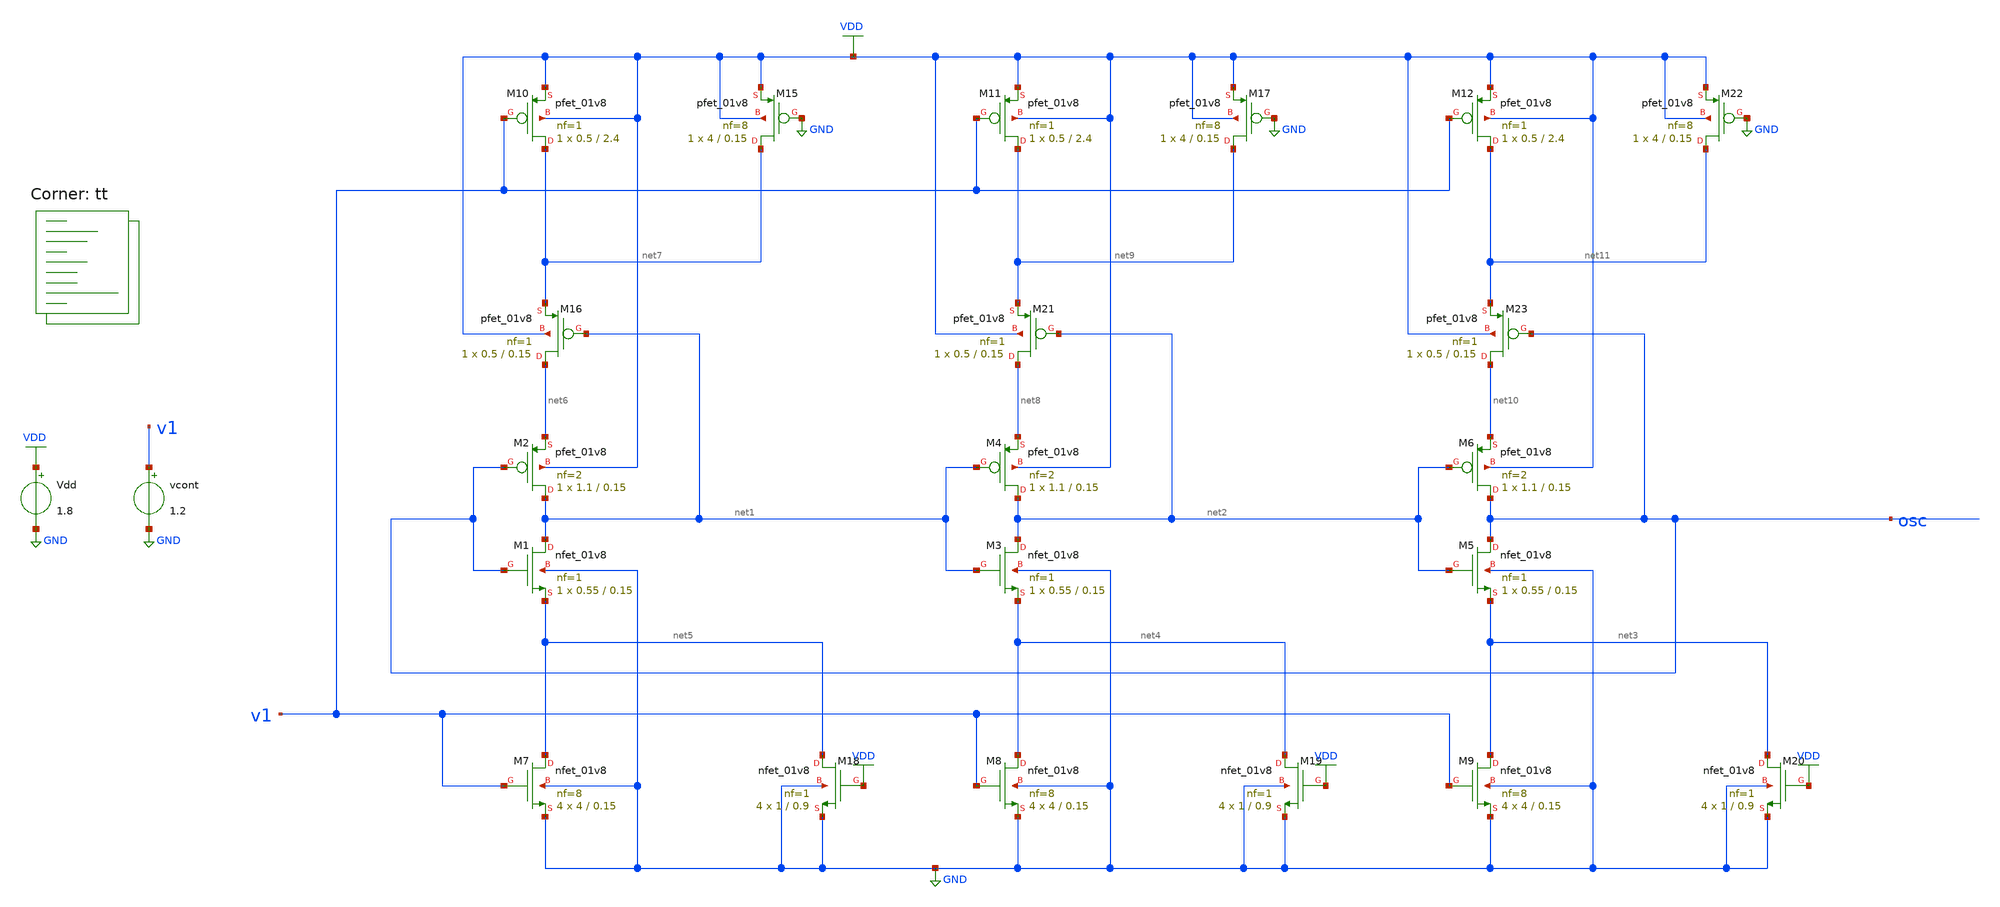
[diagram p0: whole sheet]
** sch_path: projects/pll/vco/xschem_ngspice/tb_current_starved_VCO2.sch
**.subckt tb_current_starved_VCO2
XM1 net1 osc net5 GND sky130_fd_pr__nfet_01v8 L=0.15 W=0.55 nf=1 ad='int((nf+1)/2) * W/nf * 0.29' as='int((nf+2)/2) * W/nf * 0.29'
+ pd='2*int((nf+1)/2) * (W/nf + 0.29)' ps='2*int((nf+2)/2) * (W/nf + 0.29)' nrd='0.29 / W' nrs='0.29 / W'
+ sa=0 sb=0 sd=0 mult=1 m=1
XM2 net1 osc net6 VDD sky130_fd_pr__pfet_01v8 L=0.15 W=1.1 nf=2 ad='int((nf+1)/2) * W/nf * 0.29' as='int((nf+2)/2) * W/nf * 0.29'
+ pd='2*int((nf+1)/2) * (W/nf + 0.29)' ps='2*int((nf+2)/2) * (W/nf + 0.29)' nrd='0.29 / W' nrs='0.29 / W'
+ sa=0 sb=0 sd=0 mult=1 m=1
XM3 net2 net1 net4 GND sky130_fd_pr__nfet_01v8 L=0.15 W=0.55 nf=1 ad='int((nf+1)/2) * W/nf * 0.29' as='int((nf+2)/2) * W/nf * 0.29'
+ pd='2*int((nf+1)/2) * (W/nf + 0.29)' ps='2*int((nf+2)/2) * (W/nf + 0.29)' nrd='0.29 / W' nrs='0.29 / W'
+ sa=0 sb=0 sd=0 mult=1 m=1
XM4 net2 net1 net8 VDD sky130_fd_pr__pfet_01v8 L=0.15 W=1.1 nf=2 ad='int((nf+1)/2) * W/nf * 0.29' as='int((nf+2)/2) * W/nf * 0.29'
+ pd='2*int((nf+1)/2) * (W/nf + 0.29)' ps='2*int((nf+2)/2) * (W/nf + 0.29)' nrd='0.29 / W' nrs='0.29 / W'
+ sa=0 sb=0 sd=0 mult=1 m=1
XM5 osc net2 net3 GND sky130_fd_pr__nfet_01v8 L=0.15 W=0.55 nf=1 ad='int((nf+1)/2) * W/nf * 0.29' as='int((nf+2)/2) * W/nf * 0.29'
+ pd='2*int((nf+1)/2) * (W/nf + 0.29)' ps='2*int((nf+2)/2) * (W/nf + 0.29)' nrd='0.29 / W' nrs='0.29 / W'
+ sa=0 sb=0 sd=0 mult=1 m=1
XM6 osc net2 net10 VDD sky130_fd_pr__pfet_01v8 L=0.15 W=1.1 nf=2 ad='int((nf+1)/2) * W/nf * 0.29' as='int((nf+2)/2) * W/nf * 0.29'
+ pd='2*int((nf+1)/2) * (W/nf + 0.29)' ps='2*int((nf+2)/2) * (W/nf + 0.29)' nrd='0.29 / W' nrs='0.29 / W'
+ sa=0 sb=0 sd=0 mult=1 m=1
XM7 net5 v1 GND GND sky130_fd_pr__nfet_01v8 L=0.15 W=4 nf=8 ad='int((nf+1)/2) * W/nf * 0.29' as='int((nf+2)/2) * W/nf * 0.29'
+ pd='2*int((nf+1)/2) * (W/nf + 0.29)' ps='2*int((nf+2)/2) * (W/nf + 0.29)' nrd='0.29 / W' nrs='0.29 / W'
+ sa=0 sb=0 sd=0 mult=4 m=4
XM8 net4 v1 GND GND sky130_fd_pr__nfet_01v8 L=0.15 W=4 nf=8 ad='int((nf+1)/2) * W/nf * 0.29' as='int((nf+2)/2) * W/nf * 0.29'
+ pd='2*int((nf+1)/2) * (W/nf + 0.29)' ps='2*int((nf+2)/2) * (W/nf + 0.29)' nrd='0.29 / W' nrs='0.29 / W'
+ sa=0 sb=0 sd=0 mult=4 m=4
XM9 net3 v1 GND GND sky130_fd_pr__nfet_01v8 L=0.15 W=4 nf=8 ad='int((nf+1)/2) * W/nf * 0.29' as='int((nf+2)/2) * W/nf * 0.29'
+ pd='2*int((nf+1)/2) * (W/nf + 0.29)' ps='2*int((nf+2)/2) * (W/nf + 0.29)' nrd='0.29 / W' nrs='0.29 / W'
+ sa=0 sb=0 sd=0 mult=4 m=4
XM10 net7 v1 VDD VDD sky130_fd_pr__pfet_01v8 L=2.4 W=0.5 nf=1 ad='int((nf+1)/2) * W/nf * 0.29' as='int((nf+2)/2) * W/nf * 0.29'
+ pd='2*int((nf+1)/2) * (W/nf + 0.29)' ps='2*int((nf+2)/2) * (W/nf + 0.29)' nrd='0.29 / W' nrs='0.29 / W'
+ sa=0 sb=0 sd=0 mult=1 m=1
XM11 net9 v1 VDD VDD sky130_fd_pr__pfet_01v8 L=2.4 W=0.5 nf=1 ad='int((nf+1)/2) * W/nf * 0.29' as='int((nf+2)/2) * W/nf * 0.29'
+ pd='2*int((nf+1)/2) * (W/nf + 0.29)' ps='2*int((nf+2)/2) * (W/nf + 0.29)' nrd='0.29 / W' nrs='0.29 / W'
+ sa=0 sb=0 sd=0 mult=1 m=1
XM12 net11 v1 VDD VDD sky130_fd_pr__pfet_01v8 L=2.4 W=0.5 nf=1 ad='int((nf+1)/2) * W/nf * 0.29' as='int((nf+2)/2) * W/nf * 0.29'
+ pd='2*int((nf+1)/2) * (W/nf + 0.29)' ps='2*int((nf+2)/2) * (W/nf + 0.29)' nrd='0.29 / W' nrs='0.29 / W'
+ sa=0 sb=0 sd=0 mult=1 m=1
Vdd VDD GND 1.8
vcont v1 GND 1.2
XM18 net5 VDD GND GND sky130_fd_pr__nfet_01v8 L=0.9 W=1 nf=1 ad='int((nf+1)/2) * W/nf * 0.29' as='int((nf+2)/2) * W/nf * 0.29'
+ pd='2*int((nf+1)/2) * (W/nf + 0.29)' ps='2*int((nf+2)/2) * (W/nf + 0.29)' nrd='0.29 / W' nrs='0.29 / W'
+ sa=0 sb=0 sd=0 mult=4 m=4
XM19 net4 VDD GND GND sky130_fd_pr__nfet_01v8 L=0.9 W=1 nf=1 ad='int((nf+1)/2) * W/nf * 0.29' as='int((nf+2)/2) * W/nf * 0.29'
+ pd='2*int((nf+1)/2) * (W/nf + 0.29)' ps='2*int((nf+2)/2) * (W/nf + 0.29)' nrd='0.29 / W' nrs='0.29 / W'
+ sa=0 sb=0 sd=0 mult=4 m=4
XM20 net3 VDD GND GND sky130_fd_pr__nfet_01v8 L=0.9 W=1 nf=1 ad='int((nf+1)/2) * W/nf * 0.29' as='int((nf+2)/2) * W/nf * 0.29'
+ pd='2*int((nf+1)/2) * (W/nf + 0.29)' ps='2*int((nf+2)/2) * (W/nf + 0.29)' nrd='0.29 / W' nrs='0.29 / W'
+ sa=0 sb=0 sd=0 mult=4 m=4
XM15 net7 GND VDD VDD sky130_fd_pr__pfet_01v8 L=0.15 W=4 nf=8 ad='int((nf+1)/2) * W/nf * 0.29' as='int((nf+2)/2) * W/nf * 0.29'
+ pd='2*int((nf+1)/2) * (W/nf + 0.29)' ps='2*int((nf+2)/2) * (W/nf + 0.29)' nrd='0.29 / W' nrs='0.29 / W'
+ sa=0 sb=0 sd=0 mult=1 m=1
XM16 net6 net1 net7 VDD sky130_fd_pr__pfet_01v8 L=0.15 W=0.5 nf=1 ad='int((nf+1)/2) * W/nf * 0.29' as='int((nf+2)/2) * W/nf * 0.29'
+ pd='2*int((nf+1)/2) * (W/nf + 0.29)' ps='2*int((nf+2)/2) * (W/nf + 0.29)' nrd='0.29 / W' nrs='0.29 / W'
+ sa=0 sb=0 sd=0 mult=1 m=1
XM17 net9 GND VDD VDD sky130_fd_pr__pfet_01v8 L=0.15 W=4 nf=8 ad='int((nf+1)/2) * W/nf * 0.29' as='int((nf+2)/2) * W/nf * 0.29'
+ pd='2*int((nf+1)/2) * (W/nf + 0.29)' ps='2*int((nf+2)/2) * (W/nf + 0.29)' nrd='0.29 / W' nrs='0.29 / W'
+ sa=0 sb=0 sd=0 mult=1 m=1
XM21 net8 net2 net9 VDD sky130_fd_pr__pfet_01v8 L=0.15 W=0.5 nf=1 ad='int((nf+1)/2) * W/nf * 0.29' as='int((nf+2)/2) * W/nf * 0.29'
+ pd='2*int((nf+1)/2) * (W/nf + 0.29)' ps='2*int((nf+2)/2) * (W/nf + 0.29)' nrd='0.29 / W' nrs='0.29 / W'
+ sa=0 sb=0 sd=0 mult=1 m=1
XM22 net11 GND VDD VDD sky130_fd_pr__pfet_01v8 L=0.15 W=4 nf=8 ad='int((nf+1)/2) * W/nf * 0.29' as='int((nf+2)/2) * W/nf * 0.29'
+ pd='2*int((nf+1)/2) * (W/nf + 0.29)' ps='2*int((nf+2)/2) * (W/nf + 0.29)' nrd='0.29 / W' nrs='0.29 / W'
+ sa=0 sb=0 sd=0 mult=1 m=1
XM23 net10 osc net11 VDD sky130_fd_pr__pfet_01v8 L=0.15 W=0.5 nf=1 ad='int((nf+1)/2) * W/nf * 0.29' as='int((nf+2)/2) * W/nf * 0.29'
+ pd='2*int((nf+1)/2) * (W/nf + 0.29)' ps='2*int((nf+2)/2) * (W/nf + 0.29)' nrd='0.29 / W' nrs='0.29 / W'
+ sa=0 sb=0 sd=0 mult=1 m=1
**** begin user architecture code
.lib $::SKYWATER_MODELS/sky130.lib.spice tt



.option method=gear
.option wnflag=1


*.ic v(vcont)=1.2

*.temp = 75

* Xmeasure osc freq2 measure_Kvco thresh=0.9 dir=1

.control

  * pre_osdi ./measure_Kvco.osdi

  let v_cont_start = 0.0
  let v_cont_stop = 1.9

  dowhile v_cont_start <= v_cont_stop
    alter vcont $&v_cont_start
    save v(vcont) v(osc) v(vout) v(v1) v(v2) i(vmeas) i(vmeas1)
    *save all
    tran 1ps 30ns
    remzerovec
    write tb_current_starved_VCO2_{$&v_cont_start}.raw
    * write tb_current_starved_VCO2.raw
    linearize v(osc)
    let filename = v_cont_start * 100
    wrdata /foss/designs/my_design/projects/pll/vco/xschem_ngspice/tb_current_starved_VCO2_{$&filename}.txt
+ v(osc)
    set appendwrite

    reset
    let v_cont_start = v_cont_start + 0.1
  end
.endc




**** end user architecture code
**.ends
.GLOBAL VDD
.GLOBAL GND
.end
